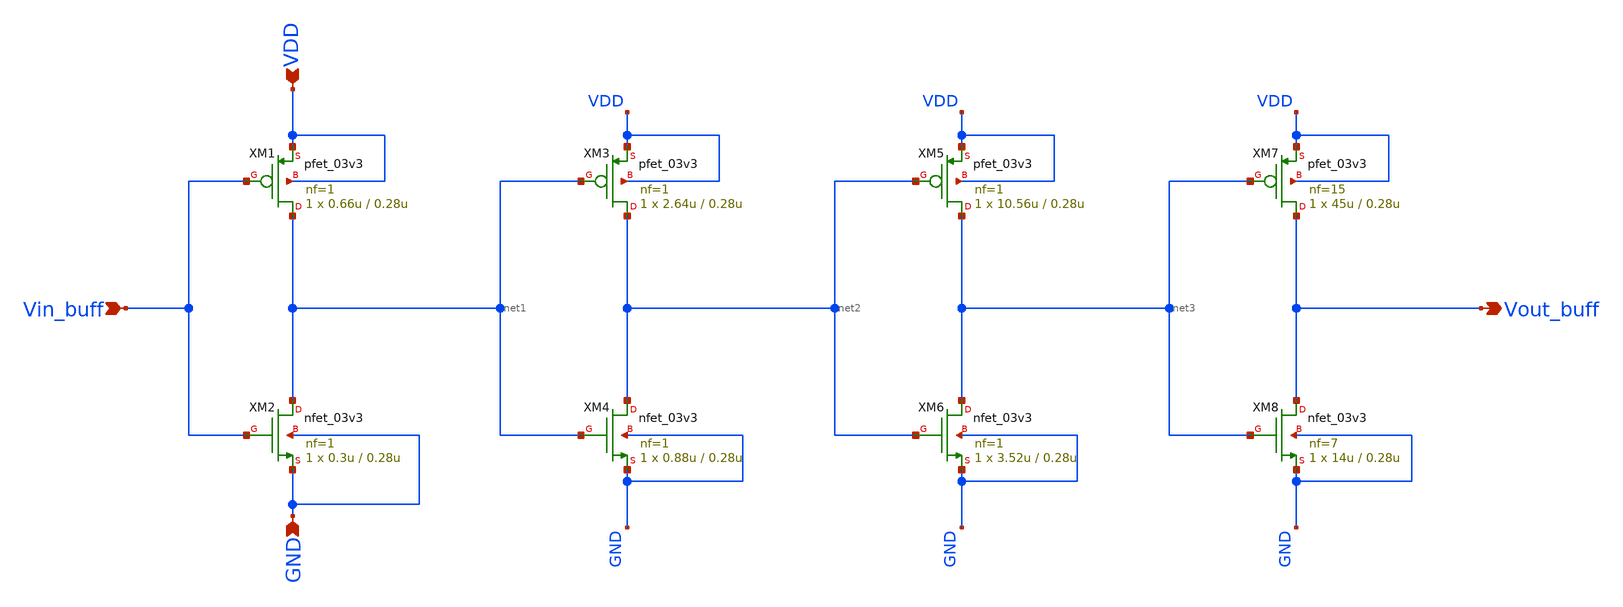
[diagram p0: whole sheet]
** sch_path: blocks/adc/lvds/buffer.sch
**.subckt buffer VDD Vin_buff Vout_buff GND
*.ipin VDD
*.ipin Vin_buff
*.opin Vout_buff
*.ipin GND
XM1 net1 Vin_buff VDD VDD pfet_03v3 L=0.28u W=0.66u nf=1 ad='int((nf+1)/2) * W/nf * 0.18u' as='int((nf+2)/2) * W/nf * 0.18u'
+ pd='2*int((nf+1)/2) * (W/nf + 0.18u)' ps='2*int((nf+2)/2) * (W/nf + 0.18u)' nrd='0.18u / W' nrs='0.18u / W'
+ sa=0 sb=0 sd=0 m=1
XM2 net1 Vin_buff GND GND nfet_03v3 L=0.28u W=0.3u nf=1 ad='int((nf+1)/2) * W/nf * 0.18u' as='int((nf+2)/2) * W/nf * 0.18u'
+ pd='2*int((nf+1)/2) * (W/nf + 0.18u)' ps='2*int((nf+2)/2) * (W/nf + 0.18u)' nrd='0.18u / W' nrs='0.18u / W'
+ sa=0 sb=0 sd=0 m=1
XM3 net2 net1 VDD VDD pfet_03v3 L=0.28u W=2.64u nf=1 ad='int((nf+1)/2) * W/nf * 0.18u' as='int((nf+2)/2) * W/nf * 0.18u'
+ pd='2*int((nf+1)/2) * (W/nf + 0.18u)' ps='2*int((nf+2)/2) * (W/nf + 0.18u)' nrd='0.18u / W' nrs='0.18u / W'
+ sa=0 sb=0 sd=0 m=1
XM4 net2 net1 GND GND nfet_03v3 L=0.28u W=0.88u nf=1 ad='int((nf+1)/2) * W/nf * 0.18u' as='int((nf+2)/2) * W/nf * 0.18u'
+ pd='2*int((nf+1)/2) * (W/nf + 0.18u)' ps='2*int((nf+2)/2) * (W/nf + 0.18u)' nrd='0.18u / W' nrs='0.18u / W'
+ sa=0 sb=0 sd=0 m=1
XM5 net3 net2 VDD VDD pfet_03v3 L=0.28u W=10.56u nf=1 ad='int((nf+1)/2) * W/nf * 0.18u' as='int((nf+2)/2) * W/nf * 0.18u'
+ pd='2*int((nf+1)/2) * (W/nf + 0.18u)' ps='2*int((nf+2)/2) * (W/nf + 0.18u)' nrd='0.18u / W' nrs='0.18u / W'
+ sa=0 sb=0 sd=0 m=1
XM6 net3 net2 GND GND nfet_03v3 L=0.28u W=3.52u nf=1 ad='int((nf+1)/2) * W/nf * 0.18u' as='int((nf+2)/2) * W/nf * 0.18u'
+ pd='2*int((nf+1)/2) * (W/nf + 0.18u)' ps='2*int((nf+2)/2) * (W/nf + 0.18u)' nrd='0.18u / W' nrs='0.18u / W'
+ sa=0 sb=0 sd=0 m=1
XM7 Vout_buff net3 VDD VDD pfet_03v3 L=0.28u W=45u nf=15 ad='int((nf+1)/2) * W/nf * 0.18u' as='int((nf+2)/2) * W/nf * 0.18u'
+ pd='2*int((nf+1)/2) * (W/nf + 0.18u)' ps='2*int((nf+2)/2) * (W/nf + 0.18u)' nrd='0.18u / W' nrs='0.18u / W'
+ sa=0 sb=0 sd=0 m=1
XM8 Vout_buff net3 GND GND nfet_03v3 L=0.28u W=14u nf=7 ad='int((nf+1)/2) * W/nf * 0.18u' as='int((nf+2)/2) * W/nf * 0.18u'
+ pd='2*int((nf+1)/2) * (W/nf + 0.18u)' ps='2*int((nf+2)/2) * (W/nf + 0.18u)' nrd='0.18u / W' nrs='0.18u / W'
+ sa=0 sb=0 sd=0 m=1
**.ends
.end
